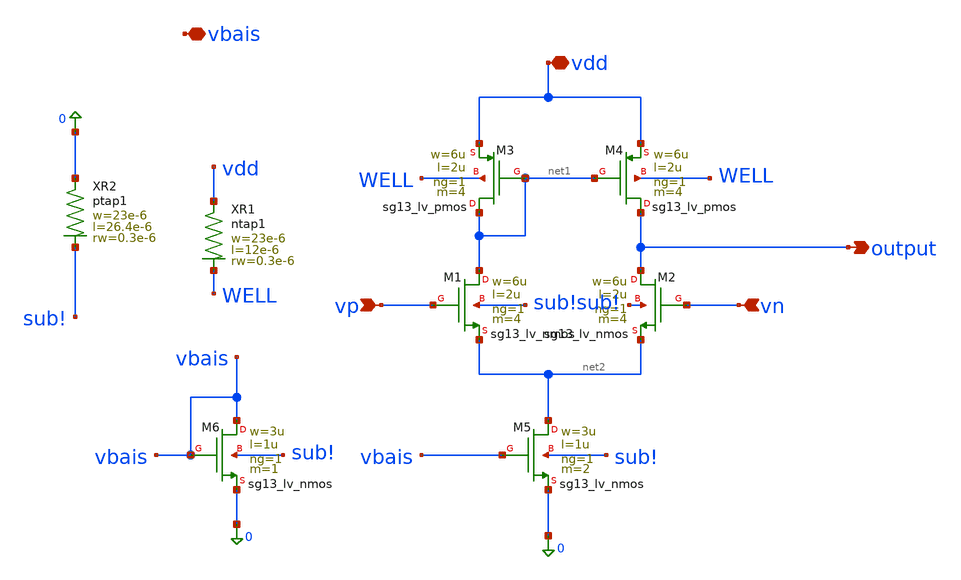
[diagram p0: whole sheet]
** sch_path: xschem/ota5stage.sch
**.subckt ota5stage vdd output vbais vp vn
*.iopin vdd
*.opin output
*.iopin vbais
*.ipin vp
*.ipin vn
XM1 net1 vp net2 sub! sg13_lv_nmos w=6u l=2u ng=1 m=4 mm_ok=1
XM2 output vn net2 sub! sg13_lv_nmos w=6u l=2u ng=1 m=4 mm_ok=1
XM3 net1 net1 vdd WELL sg13_lv_pmos w=6u l=2u ng=1 m=4 mm_ok=1
XM4 output net1 vdd WELL sg13_lv_pmos w=6u l=2u ng=1 m=4 mm_ok=1
XM5 net2 vbais 0 sub! sg13_lv_nmos w=3u l=1u ng=1 m=2 mm_ok=1
XR1 vdd WELL ntap1 R=3.313 w=23e-6 l=12e-6 rw=0.3e-6
XR2 0 sub! ptap1 R=2.335 w=23e-6 l=26.4e-6 rw=0.3e-6
XM6 vbais vbais 0 sub! sg13_lv_nmos w=3u l=1u ng=1 m=1 mm_ok=1
**.ends
.end
